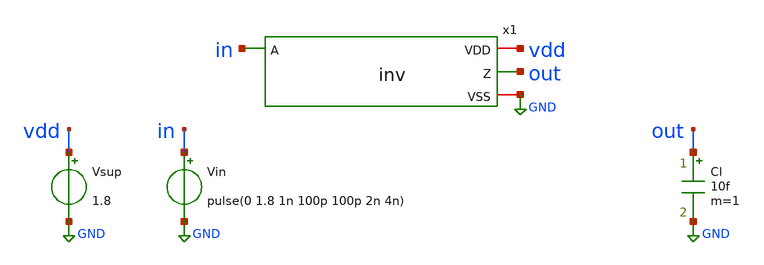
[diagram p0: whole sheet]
** sch_path: pipeline/analog/inv/inv_tb.sch
**.subckt inv_tb
x1 in vdd out GND inv
Vsup vdd GND 1.8
Vin in GND pulse(0 1.8 1n 100p 100p 2n 4n)
Cl out GND 10f m=1
**** begin user architecture code


%PDK_LIB%



.param W_P=1.0 W_N=0.5 L_P=0.15 L_N=0.15
.control
dc Vin 0 1.8 0.01
meas dc vtrip WHEN v(out)=0.9 FALL=1
tran 10p 8n
meas tran tphl TRIG v(in) VAL=0.9 RISE=1 TARG v(out) VAL=0.9 FALL=1
meas tran tplh TRIG v(in) VAL=0.9 FALL=1 TARG v(out) VAL=0.9 RISE=1
meas tran ivdd_avg AVG i(Vsup) FROM=0 TO=8n
quit
.endc


**** end user architecture code
**.ends

* expanding   symbol:  inv.sym # of pins=4
** sym_path: pipeline/analog/inv/inv.sym
** sch_path: pipeline/analog/inv/inv.sch
.subckt inv A VDD Z VSS
*.ipin A
*.opin Z
*.iopin VDD
*.iopin VSS
XM1 Z A VSS VSS sky130_fd_pr__nfet_01v8 L=L_N W=W_N nf=1 ad='int((nf+1)/2) * W/nf * 0.29' as='int((nf+2)/2) * W/nf * 0.29'
+ pd='2*int((nf+1)/2) * (W/nf + 0.29)' ps='2*int((nf+2)/2) * (W/nf + 0.29)' nrd='0.29 / W' nrs='0.29 / W'
+ sa=0 sb=0 sd=0 mult=1 m=1
XM2 Z A VDD VDD sky130_fd_pr__pfet_01v8 L=L_P W=W_P nf=1 ad='int((nf+1)/2) * W/nf * 0.29' as='int((nf+2)/2) * W/nf * 0.29'
+ pd='2*int((nf+1)/2) * (W/nf + 0.29)' ps='2*int((nf+2)/2) * (W/nf + 0.29)' nrd='0.29 / W' nrs='0.29 / W'
+ sa=0 sb=0 sd=0 mult=1 m=1
.ends

.GLOBAL GND
.end
